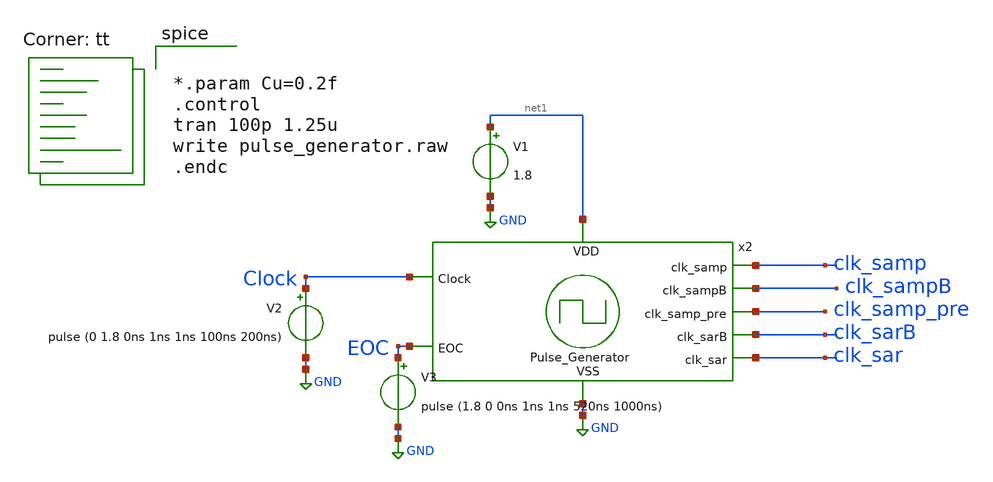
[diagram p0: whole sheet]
** sch_path: Pulse_Generator_tb.sch
**.subckt Pulse_Generator_tb
V1 net1 GND 1.8
V2 Clock GND pulse (0 1.8 0ns 1ns 1ns 100ns 200ns)
V3 EOC GND pulse (1.8 0 0ns 1ns 1ns 520ns 1000ns)
x2 net1 Clock clk_samp clk_sampB clk_samp_pre clk_sarB EOC clk_sar GND Pulse_Generator
**** begin user architecture code
.lib $::SKYWATER_MODELS/sky130.lib.spice tt


*.param Cu=0.2f
.control
tran 100p 1.25u
write pulse_generator.raw
.endc


**** end user architecture code
**.ends

* expanding   symbol:  Pulse_Generator.sym # of pins=9
** sym_path: Pulse_Generator.sym
** sch_path: Pulse_Generator.sch
.subckt Pulse_Generator VDD Clock clk_samp clk_sampB clk_samp_pre clk_sarB EOC clk_sar VSS
*.ipin Clock
*.ipin VDD
*.opin clk_sampB
*.opin clk_sar
*.ipin VSS
*.ipin EOC
*.opin clk_sarB
*.opin clk_samp
*.opin clk_samp_pre
x1 VDD VSS net4 Clock net1 xor
x2 VDD net3 net1 VSS Delay_cell
x3 VDD net2 net4 Clock VSS nand
x5 VDD VSS net5 net2 net6 VDD FFD_RSpin
x6 VDD net8 net5 VSS Delay_cell
x7 VSS VDD net7 clk_samp_pre VSS net6 MUX_2to1
x8 VSS VDD net9 EOC VSS net7 MUX_2to1
x9 VDD net10 net3 VSS Delay_cell
x13 VDD net9 clk_sarB VSS Inverter
x14 VDD clk_sarB clk_sar VSS Inverter
x4 VDD net2 clk_samp_pre VSS INV_PG
x15 VDD clk_samp_pre clk_sampB VSS INV_PG
x16 VDD clk_sampB clk_samp VSS INV_PG
x17 VDD net11 net10 VSS Delay_cell
x18 VDD Clock net11 VSS Delay_cell
x19 VDD clk_sar net8 VSS Delay_cell
.ends


* expanding   symbol:  xor.sym # of pins=5
** sym_path: xor.sym
** sch_path: xor.sch
.subckt xor VDD VSS Y A B
*.ipin A
*.ipin VDD
*.opin Y
*.ipin B
*.ipin VSS
XM1 net1 A VDD VDD sky130_fd_pr__pfet_01v8 L=0.15 W=2 nf=1 ad='int((nf+1)/2) * W/nf * 0.29' as='int((nf+2)/2) * W/nf * 0.29'
+ pd='2*int((nf+1)/2) * (W/nf + 0.29)' ps='2*int((nf+2)/2) * (W/nf + 0.29)' nrd='0.29 / W' nrs='0.29 / W'
+ sa=0 sb=0 sd=0 mult=1 m=1
XM2 Y A_bar net1 VDD sky130_fd_pr__pfet_01v8 L=0.15 W=2 nf=1 ad='int((nf+1)/2) * W/nf * 0.29' as='int((nf+2)/2) * W/nf * 0.29'
+ pd='2*int((nf+1)/2) * (W/nf + 0.29)' ps='2*int((nf+2)/2) * (W/nf + 0.29)' nrd='0.29 / W' nrs='0.29 / W'
+ sa=0 sb=0 sd=0 mult=1 m=1
XM3 net1 B VDD VDD sky130_fd_pr__pfet_01v8 L=0.15 W=2 nf=1 ad='int((nf+1)/2) * W/nf * 0.29' as='int((nf+2)/2) * W/nf * 0.29'
+ pd='2*int((nf+1)/2) * (W/nf + 0.29)' ps='2*int((nf+2)/2) * (W/nf + 0.29)' nrd='0.29 / W' nrs='0.29 / W'
+ sa=0 sb=0 sd=0 mult=1 m=1
XM4 Y B_bar net1 VDD sky130_fd_pr__pfet_01v8 L=0.15 W=2 nf=1 ad='int((nf+1)/2) * W/nf * 0.29' as='int((nf+2)/2) * W/nf * 0.29'
+ pd='2*int((nf+1)/2) * (W/nf + 0.29)' ps='2*int((nf+2)/2) * (W/nf + 0.29)' nrd='0.29 / W' nrs='0.29 / W'
+ sa=0 sb=0 sd=0 mult=1 m=1
XM5 Y A net2 VSS sky130_fd_pr__nfet_01v8 L=0.15 W=1 nf=1 ad='int((nf+1)/2) * W/nf * 0.29' as='int((nf+2)/2) * W/nf * 0.29'
+ pd='2*int((nf+1)/2) * (W/nf + 0.29)' ps='2*int((nf+2)/2) * (W/nf + 0.29)' nrd='0.29 / W' nrs='0.29 / W'
+ sa=0 sb=0 sd=0 mult=1 m=1
XM6 net2 B VSS VSS sky130_fd_pr__nfet_01v8 L=0.15 W=1 nf=1 ad='int((nf+1)/2) * W/nf * 0.29' as='int((nf+2)/2) * W/nf * 0.29'
+ pd='2*int((nf+1)/2) * (W/nf + 0.29)' ps='2*int((nf+2)/2) * (W/nf + 0.29)' nrd='0.29 / W' nrs='0.29 / W'
+ sa=0 sb=0 sd=0 mult=1 m=1
XM7 Y A_bar net3 VSS sky130_fd_pr__nfet_01v8 L=0.15 W=1 nf=1 ad='int((nf+1)/2) * W/nf * 0.29' as='int((nf+2)/2) * W/nf * 0.29'
+ pd='2*int((nf+1)/2) * (W/nf + 0.29)' ps='2*int((nf+2)/2) * (W/nf + 0.29)' nrd='0.29 / W' nrs='0.29 / W'
+ sa=0 sb=0 sd=0 mult=1 m=1
XM8 net3 B_bar VSS VSS sky130_fd_pr__nfet_01v8 L=0.15 W=1 nf=1 ad='int((nf+1)/2) * W/nf * 0.29' as='int((nf+2)/2) * W/nf * 0.29'
+ pd='2*int((nf+1)/2) * (W/nf + 0.29)' ps='2*int((nf+2)/2) * (W/nf + 0.29)' nrd='0.29 / W' nrs='0.29 / W'
+ sa=0 sb=0 sd=0 mult=1 m=1
XM9 A_bar A VSS VSS sky130_fd_pr__nfet_01v8 L=0.15 W=1 nf=1 ad='int((nf+1)/2) * W/nf * 0.29' as='int((nf+2)/2) * W/nf * 0.29'
+ pd='2*int((nf+1)/2) * (W/nf + 0.29)' ps='2*int((nf+2)/2) * (W/nf + 0.29)' nrd='0.29 / W' nrs='0.29 / W'
+ sa=0 sb=0 sd=0 mult=1 m=1
XM10 A_bar A VDD VDD sky130_fd_pr__pfet_01v8 L=0.15 W=2 nf=1 ad='int((nf+1)/2) * W/nf * 0.29' as='int((nf+2)/2) * W/nf * 0.29'
+ pd='2*int((nf+1)/2) * (W/nf + 0.29)' ps='2*int((nf+2)/2) * (W/nf + 0.29)' nrd='0.29 / W' nrs='0.29 / W'
+ sa=0 sb=0 sd=0 mult=1 m=1
XM11 B_bar B VSS VSS sky130_fd_pr__nfet_01v8 L=0.15 W=1 nf=1 ad='int((nf+1)/2) * W/nf * 0.29' as='int((nf+2)/2) * W/nf * 0.29'
+ pd='2*int((nf+1)/2) * (W/nf + 0.29)' ps='2*int((nf+2)/2) * (W/nf + 0.29)' nrd='0.29 / W' nrs='0.29 / W'
+ sa=0 sb=0 sd=0 mult=1 m=1
XM12 B_bar B VDD VDD sky130_fd_pr__pfet_01v8 L=0.15 W=2 nf=1 ad='int((nf+1)/2) * W/nf * 0.29' as='int((nf+2)/2) * W/nf * 0.29'
+ pd='2*int((nf+1)/2) * (W/nf + 0.29)' ps='2*int((nf+2)/2) * (W/nf + 0.29)' nrd='0.29 / W' nrs='0.29 / W'
+ sa=0 sb=0 sd=0 mult=1 m=1
.ends


* expanding   symbol:  Delay_cell.sym # of pins=4
** sym_path: Delay_cell.sym
** sch_path: Delay_cell.sch
.subckt Delay_cell VDD IN OUT VSS
*.ipin IN
*.ipin VSS
*.ipin VDD
*.opin OUT
XM3 net1 IN VSS VSS sky130_fd_pr__nfet_01v8 L=0.3 W=6 nf=1 ad='int((nf+1)/2) * W/nf * 0.29' as='int((nf+2)/2) * W/nf * 0.29'
+ pd='2*int((nf+1)/2) * (W/nf + 0.29)' ps='2*int((nf+2)/2) * (W/nf + 0.29)' nrd='0.29 / W' nrs='0.29 / W'
+ sa=0 sb=0 sd=0 mult=1 m=1
XM4 net1 IN VDD VDD sky130_fd_pr__pfet_01v8 L=0.3 W=12 nf=1 ad='int((nf+1)/2) * W/nf * 0.29' as='int((nf+2)/2) * W/nf * 0.29'
+ pd='2*int((nf+1)/2) * (W/nf + 0.29)' ps='2*int((nf+2)/2) * (W/nf + 0.29)' nrd='0.29 / W' nrs='0.29 / W'
+ sa=0 sb=0 sd=0 mult=1 m=1
XM5 net2 net1 VSS VSS sky130_fd_pr__nfet_01v8 L=0.3 W=6 nf=1 ad='int((nf+1)/2) * W/nf * 0.29' as='int((nf+2)/2) * W/nf * 0.29'
+ pd='2*int((nf+1)/2) * (W/nf + 0.29)' ps='2*int((nf+2)/2) * (W/nf + 0.29)' nrd='0.29 / W' nrs='0.29 / W'
+ sa=0 sb=0 sd=0 mult=1 m=1
XM6 net2 net1 VDD VDD sky130_fd_pr__pfet_01v8 L=0.3 W=12 nf=1 ad='int((nf+1)/2) * W/nf * 0.29' as='int((nf+2)/2) * W/nf * 0.29'
+ pd='2*int((nf+1)/2) * (W/nf + 0.29)' ps='2*int((nf+2)/2) * (W/nf + 0.29)' nrd='0.29 / W' nrs='0.29 / W'
+ sa=0 sb=0 sd=0 mult=1 m=1
XM7 net3 net2 VSS VSS sky130_fd_pr__nfet_01v8 L=0.3 W=6 nf=1 ad='int((nf+1)/2) * W/nf * 0.29' as='int((nf+2)/2) * W/nf * 0.29'
+ pd='2*int((nf+1)/2) * (W/nf + 0.29)' ps='2*int((nf+2)/2) * (W/nf + 0.29)' nrd='0.29 / W' nrs='0.29 / W'
+ sa=0 sb=0 sd=0 mult=1 m=1
XM8 net3 net2 VDD VDD sky130_fd_pr__pfet_01v8 L=0.3 W=12 nf=1 ad='int((nf+1)/2) * W/nf * 0.29' as='int((nf+2)/2) * W/nf * 0.29'
+ pd='2*int((nf+1)/2) * (W/nf + 0.29)' ps='2*int((nf+2)/2) * (W/nf + 0.29)' nrd='0.29 / W' nrs='0.29 / W'
+ sa=0 sb=0 sd=0 mult=1 m=1
XM9 OUT net3 VSS VSS sky130_fd_pr__nfet_01v8 L=0.3 W=6 nf=1 ad='int((nf+1)/2) * W/nf * 0.29' as='int((nf+2)/2) * W/nf * 0.29'
+ pd='2*int((nf+1)/2) * (W/nf + 0.29)' ps='2*int((nf+2)/2) * (W/nf + 0.29)' nrd='0.29 / W' nrs='0.29 / W'
+ sa=0 sb=0 sd=0 mult=1 m=1
XM10 OUT net3 VDD VDD sky130_fd_pr__pfet_01v8 L=0.3 W=12 nf=1 ad='int((nf+1)/2) * W/nf * 0.29' as='int((nf+2)/2) * W/nf * 0.29'
+ pd='2*int((nf+1)/2) * (W/nf + 0.29)' ps='2*int((nf+2)/2) * (W/nf + 0.29)' nrd='0.29 / W' nrs='0.29 / W'
+ sa=0 sb=0 sd=0 mult=1 m=1
XC1 net1 VSS sky130_fd_pr__cap_mim_m3_1 W=9.8 L=9.8 MF=4 m=4
XC2 net2 VSS sky130_fd_pr__cap_mim_m3_1 W=9.8 L=9.8 MF=4 m=4
XC3 net3 VSS sky130_fd_pr__cap_mim_m3_1 W=9.8 L=9.8 MF=4 m=4
.ends


* expanding   symbol:  nand.sym # of pins=5
** sym_path: nand.sym
** sch_path: nand.sch
.subckt nand VDD Y A B VSS
*.ipin VDD
*.ipin A
*.ipin B
*.ipin VSS
*.opin Y
XM1 Y A net1 VSS sky130_fd_pr__nfet_01v8 L=0.15 W=0.5 nf=1 ad='int((nf+1)/2) * W/nf * 0.29' as='int((nf+2)/2) * W/nf * 0.29'
+ pd='2*int((nf+1)/2) * (W/nf + 0.29)' ps='2*int((nf+2)/2) * (W/nf + 0.29)' nrd='0.29 / W' nrs='0.29 / W'
+ sa=0 sb=0 sd=0 mult=1 m=1
XM2 net1 B VSS VSS sky130_fd_pr__nfet_01v8 L=0.15 W=0.5 nf=1 ad='int((nf+1)/2) * W/nf * 0.29' as='int((nf+2)/2) * W/nf * 0.29'
+ pd='2*int((nf+1)/2) * (W/nf + 0.29)' ps='2*int((nf+2)/2) * (W/nf + 0.29)' nrd='0.29 / W' nrs='0.29 / W'
+ sa=0 sb=0 sd=0 mult=1 m=1
XM3 Y A VDD VDD sky130_fd_pr__pfet_01v8 L=0.15 W=1.5 nf=1 ad='int((nf+1)/2) * W/nf * 0.29' as='int((nf+2)/2) * W/nf * 0.29'
+ pd='2*int((nf+1)/2) * (W/nf + 0.29)' ps='2*int((nf+2)/2) * (W/nf + 0.29)' nrd='0.29 / W' nrs='0.29 / W'
+ sa=0 sb=0 sd=0 mult=1 m=1
XM4 Y B VDD VDD sky130_fd_pr__pfet_01v8 L=0.15 W=1.5 nf=1 ad='int((nf+1)/2) * W/nf * 0.29' as='int((nf+2)/2) * W/nf * 0.29'
+ pd='2*int((nf+1)/2) * (W/nf + 0.29)' ps='2*int((nf+2)/2) * (W/nf + 0.29)' nrd='0.29 / W' nrs='0.29 / W'
+ sa=0 sb=0 sd=0 mult=1 m=1
.ends


* expanding   symbol:  FFD_RSpin.sym # of pins=6
** sym_path: FFD_RSpin.sym
** sch_path: FFD_RSpin.sch
.subckt FFD_RSpin VDD VSS RESET CLOCK Q D
*.ipin CLOCK
*.ipin D
*.ipin RESET
*.ipin VDD
*.ipin VSS
*.opin Q
XM1 D CLKB net1 VSS sky130_fd_pr__nfet_01v8 L=0.15 W=0.5 nf=1 ad='int((nf+1)/2) * W/nf * 0.29' as='int((nf+2)/2) * W/nf * 0.29'
+ pd='2*int((nf+1)/2) * (W/nf + 0.29)' ps='2*int((nf+2)/2) * (W/nf + 0.29)' nrd='0.29 / W' nrs='0.29 / W'
+ sa=0 sb=0 sd=0 mult=1 m=1
XM2 D CLK net1 VDD sky130_fd_pr__pfet_01v8 L=0.15 W=1 nf=1 ad='int((nf+1)/2) * W/nf * 0.29' as='int((nf+2)/2) * W/nf * 0.29'
+ pd='2*int((nf+1)/2) * (W/nf + 0.29)' ps='2*int((nf+2)/2) * (W/nf + 0.29)' nrd='0.29 / W' nrs='0.29 / W'
+ sa=0 sb=0 sd=0 mult=1 m=1
XM3 net2 CLK net3 VSS sky130_fd_pr__nfet_01v8 L=0.15 W=0.5 nf=1 ad='int((nf+1)/2) * W/nf * 0.29' as='int((nf+2)/2) * W/nf * 0.29'
+ pd='2*int((nf+1)/2) * (W/nf + 0.29)' ps='2*int((nf+2)/2) * (W/nf + 0.29)' nrd='0.29 / W' nrs='0.29 / W'
+ sa=0 sb=0 sd=0 mult=1 m=1
XM4 net2 CLKB net3 VDD sky130_fd_pr__pfet_01v8 L=0.15 W=1 nf=1 ad='int((nf+1)/2) * W/nf * 0.29' as='int((nf+2)/2) * W/nf * 0.29'
+ pd='2*int((nf+1)/2) * (W/nf + 0.29)' ps='2*int((nf+2)/2) * (W/nf + 0.29)' nrd='0.29 / W' nrs='0.29 / W'
+ sa=0 sb=0 sd=0 mult=1 m=1
XM5 net1 CLK net5 VSS sky130_fd_pr__nfet_01v8 L=0.15 W=0.5 nf=1 ad='int((nf+1)/2) * W/nf * 0.29' as='int((nf+2)/2) * W/nf * 0.29'
+ pd='2*int((nf+1)/2) * (W/nf + 0.29)' ps='2*int((nf+2)/2) * (W/nf + 0.29)' nrd='0.29 / W' nrs='0.29 / W'
+ sa=0 sb=0 sd=0 mult=1 m=1
XM6 net1 CLKB net5 VDD sky130_fd_pr__pfet_01v8 L=0.15 W=1 nf=1 ad='int((nf+1)/2) * W/nf * 0.29' as='int((nf+2)/2) * W/nf * 0.29'
+ pd='2*int((nf+1)/2) * (W/nf + 0.29)' ps='2*int((nf+2)/2) * (W/nf + 0.29)' nrd='0.29 / W' nrs='0.29 / W'
+ sa=0 sb=0 sd=0 mult=1 m=1
XM7 net3 CLKB net6 VSS sky130_fd_pr__nfet_01v8 L=0.15 W=0.5 nf=1 ad='int((nf+1)/2) * W/nf * 0.29' as='int((nf+2)/2) * W/nf * 0.29'
+ pd='2*int((nf+1)/2) * (W/nf + 0.29)' ps='2*int((nf+2)/2) * (W/nf + 0.29)' nrd='0.29 / W' nrs='0.29 / W'
+ sa=0 sb=0 sd=0 mult=1 m=1
XM8 net3 CLK net6 VDD sky130_fd_pr__pfet_01v8 L=0.15 W=1 nf=1 ad='int((nf+1)/2) * W/nf * 0.29' as='int((nf+2)/2) * W/nf * 0.29'
+ pd='2*int((nf+1)/2) * (W/nf + 0.29)' ps='2*int((nf+2)/2) * (W/nf + 0.29)' nrd='0.29 / W' nrs='0.29 / W'
+ sa=0 sb=0 sd=0 mult=1 m=1
x2 VDD RESET net3 net4 VSS nor_FFD
x3 VDD RESET net1 net2 VSS nor_FFD
x7 VDD CLOCK CLKB VSS Inverter
x8 VDD CLKB CLK VSS Inverter
x1 VDD net4 net7 VSS Inverter
x4 VDD net7 Q VSS Inverter
x5 VDD net2 net5 VSS Inverter
x6 VDD net4 net6 VSS Inverter
.ends


* expanding   symbol:  MUX_2to1.sym # of pins=6
** sym_path: MUX_2to1.sym
** sch_path: MUX_2to1.sch
.subckt MUX_2to1 in1 VDD out select VSS in0
*.ipin select
*.ipin VSS
*.ipin VDD
*.ipin in1
*.ipin in0
*.opin out
XM1 net1 select VSS VSS sky130_fd_pr__nfet_01v8 L=0.15 W=1 nf=1 ad='int((nf+1)/2) * W/nf * 0.29' as='int((nf+2)/2) * W/nf * 0.29'
+ pd='2*int((nf+1)/2) * (W/nf + 0.29)' ps='2*int((nf+2)/2) * (W/nf + 0.29)' nrd='0.29 / W' nrs='0.29 / W'
+ sa=0 sb=0 sd=0 mult=1 m=1
XM2 net1 select VDD VDD sky130_fd_pr__pfet_01v8 L=0.15 W=2 nf=1 ad='int((nf+1)/2) * W/nf * 0.29' as='int((nf+2)/2) * W/nf * 0.29'
+ pd='2*int((nf+1)/2) * (W/nf + 0.29)' ps='2*int((nf+2)/2) * (W/nf + 0.29)' nrd='0.29 / W' nrs='0.29 / W'
+ sa=0 sb=0 sd=0 mult=1 m=1
XM3 out select in1 VSS sky130_fd_pr__nfet_01v8 L=0.15 W=3 nf=1 ad='int((nf+1)/2) * W/nf * 0.29' as='int((nf+2)/2) * W/nf * 0.29'
+ pd='2*int((nf+1)/2) * (W/nf + 0.29)' ps='2*int((nf+2)/2) * (W/nf + 0.29)' nrd='0.29 / W' nrs='0.29 / W'
+ sa=0 sb=0 sd=0 mult=1 m=1
XM4 out net1 in1 VDD sky130_fd_pr__pfet_01v8 L=0.15 W=3 nf=1 ad='int((nf+1)/2) * W/nf * 0.29' as='int((nf+2)/2) * W/nf * 0.29'
+ pd='2*int((nf+1)/2) * (W/nf + 0.29)' ps='2*int((nf+2)/2) * (W/nf + 0.29)' nrd='0.29 / W' nrs='0.29 / W'
+ sa=0 sb=0 sd=0 mult=1 m=1
XM5 out net1 in0 VSS sky130_fd_pr__nfet_01v8 L=0.15 W=3 nf=1 ad='int((nf+1)/2) * W/nf * 0.29' as='int((nf+2)/2) * W/nf * 0.29'
+ pd='2*int((nf+1)/2) * (W/nf + 0.29)' ps='2*int((nf+2)/2) * (W/nf + 0.29)' nrd='0.29 / W' nrs='0.29 / W'
+ sa=0 sb=0 sd=0 mult=1 m=1
XM6 out select in0 VDD sky130_fd_pr__pfet_01v8 L=0.15 W=3 nf=1 ad='int((nf+1)/2) * W/nf * 0.29' as='int((nf+2)/2) * W/nf * 0.29'
+ pd='2*int((nf+1)/2) * (W/nf + 0.29)' ps='2*int((nf+2)/2) * (W/nf + 0.29)' nrd='0.29 / W' nrs='0.29 / W'
+ sa=0 sb=0 sd=0 mult=1 m=1
.ends


* expanding   symbol:  Inverter.sym # of pins=4
** sym_path: Inverter.sym
** sch_path: Inverter.sch
.subckt Inverter VDD IN OUT VSS
*.ipin IN
*.ipin VSS
*.ipin VDD
*.opin OUT
XM1 OUT IN VSS VSS sky130_fd_pr__nfet_01v8 L=0.3 W=1 nf=1 ad='int((nf+1)/2) * W/nf * 0.29' as='int((nf+2)/2) * W/nf * 0.29'
+ pd='2*int((nf+1)/2) * (W/nf + 0.29)' ps='2*int((nf+2)/2) * (W/nf + 0.29)' nrd='0.29 / W' nrs='0.29 / W'
+ sa=0 sb=0 sd=0 mult=1 m=1
XM2 OUT IN VDD VDD sky130_fd_pr__pfet_01v8 L=0.3 W=2 nf=1 ad='int((nf+1)/2) * W/nf * 0.29' as='int((nf+2)/2) * W/nf * 0.29'
+ pd='2*int((nf+1)/2) * (W/nf + 0.29)' ps='2*int((nf+2)/2) * (W/nf + 0.29)' nrd='0.29 / W' nrs='0.29 / W'
+ sa=0 sb=0 sd=0 mult=1 m=1
.ends


* expanding   symbol:  INV_PG.sym # of pins=4
** sym_path: INV_PG.sym
** sch_path: INV_PG.sch
.subckt INV_PG VDD IN OUT VSS
*.ipin IN
*.ipin VSS
*.ipin VDD
*.opin OUT
XM1 OUT IN VSS VSS sky130_fd_pr__nfet_01v8 L=0.3 W=5 nf=1 ad='int((nf+1)/2) * W/nf * 0.29' as='int((nf+2)/2) * W/nf * 0.29'
+ pd='2*int((nf+1)/2) * (W/nf + 0.29)' ps='2*int((nf+2)/2) * (W/nf + 0.29)' nrd='0.29 / W' nrs='0.29 / W'
+ sa=0 sb=0 sd=0 mult=1 m=1
XM2 OUT IN VDD VDD sky130_fd_pr__pfet_01v8 L=0.3 W=8 nf=1 ad='int((nf+1)/2) * W/nf * 0.29' as='int((nf+2)/2) * W/nf * 0.29'
+ pd='2*int((nf+1)/2) * (W/nf + 0.29)' ps='2*int((nf+2)/2) * (W/nf + 0.29)' nrd='0.29 / W' nrs='0.29 / W'
+ sa=0 sb=0 sd=0 mult=1 m=1
.ends


* expanding   symbol:  nor_FFD.sym # of pins=5
** sym_path: nor_FFD.sym
** sch_path: nor_FFD.sch
.subckt nor_FFD VDD A B Y VSS
*.ipin VDD
*.ipin A
*.ipin B
*.ipin VSS
*.opin Y
XM1 Y A VSS VSS sky130_fd_pr__nfet_01v8 L=0.15 W=0.5 nf=1 ad='int((nf+1)/2) * W/nf * 0.29' as='int((nf+2)/2) * W/nf * 0.29'
+ pd='2*int((nf+1)/2) * (W/nf + 0.29)' ps='2*int((nf+2)/2) * (W/nf + 0.29)' nrd='0.29 / W' nrs='0.29 / W'
+ sa=0 sb=0 sd=0 mult=1 m=1
XM2 Y B VSS VSS sky130_fd_pr__nfet_01v8 L=0.15 W=0.5 nf=1 ad='int((nf+1)/2) * W/nf * 0.29' as='int((nf+2)/2) * W/nf * 0.29'
+ pd='2*int((nf+1)/2) * (W/nf + 0.29)' ps='2*int((nf+2)/2) * (W/nf + 0.29)' nrd='0.29 / W' nrs='0.29 / W'
+ sa=0 sb=0 sd=0 mult=1 m=1
XM3 net1 A VDD VDD sky130_fd_pr__pfet_01v8 L=0.15 W=2.5 nf=1 ad='int((nf+1)/2) * W/nf * 0.29' as='int((nf+2)/2) * W/nf * 0.29'
+ pd='2*int((nf+1)/2) * (W/nf + 0.29)' ps='2*int((nf+2)/2) * (W/nf + 0.29)' nrd='0.29 / W' nrs='0.29 / W'
+ sa=0 sb=0 sd=0 mult=1 m=1
XM4 Y B net1 VDD sky130_fd_pr__pfet_01v8 L=0.15 W=2.5 nf=1 ad='int((nf+1)/2) * W/nf * 0.29' as='int((nf+2)/2) * W/nf * 0.29'
+ pd='2*int((nf+1)/2) * (W/nf + 0.29)' ps='2*int((nf+2)/2) * (W/nf + 0.29)' nrd='0.29 / W' nrs='0.29 / W'
+ sa=0 sb=0 sd=0 mult=1 m=1
.ends

.GLOBAL GND
.end
